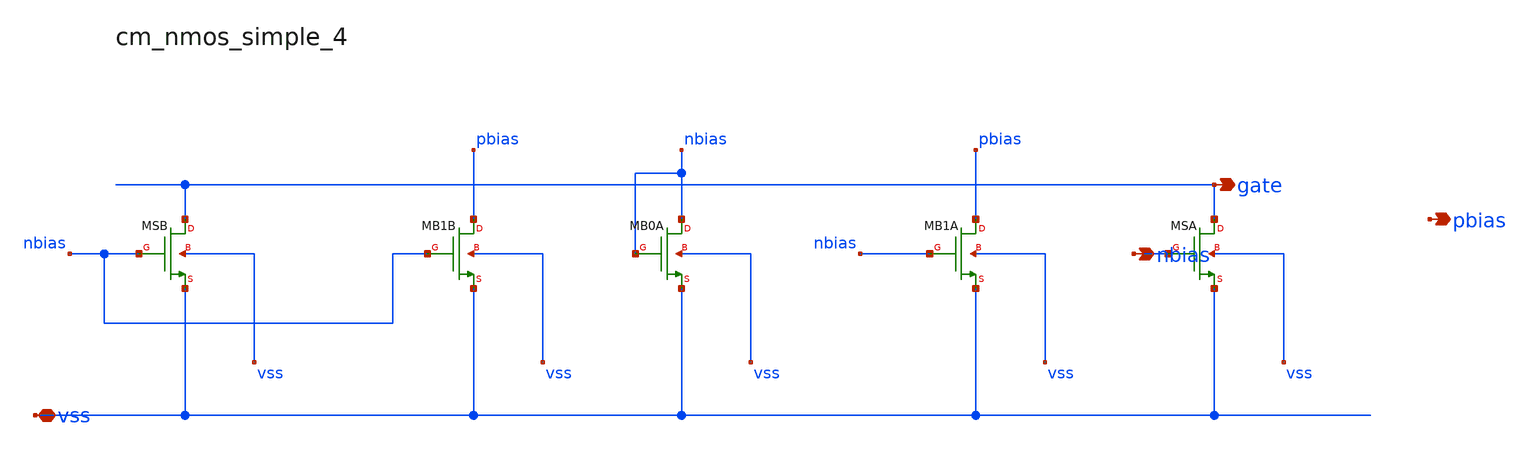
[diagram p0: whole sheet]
** sch_path: analog-db/raw/ldo_010_capless_lowiq/hier/blocks/cm_nmos_simple_4.sch
**.subckt cm_nmos_simple_4 vss gate nbias pbias
*.iopin vss
*.opin gate
*.opin nbias
*.opin pbias
XMB0A nbias nbias vss vss sg13_lv_nmos w={x_dut_xmb0_w/2} l=x_dut_xmb0_l ng=1 m=1
XMB1A pbias nbias vss vss sg13_lv_nmos w={x_dut_xmb1_w/2} l=x_dut_xmb0_l ng=1 m=1
XMB1B pbias nbias vss vss sg13_lv_nmos w={x_dut_xmb1_w/2} l=x_dut_xmb0_l ng=1 m=1
XMSA gate nbias vss vss sg13_lv_nmos w={x_dut_xms_w/2} l=x_dut_xms_l ng=1 m=1
XMSB gate nbias vss vss sg13_lv_nmos w={x_dut_xms_w/2} l=x_dut_xms_l ng=1 m=1
**.ends
.end
